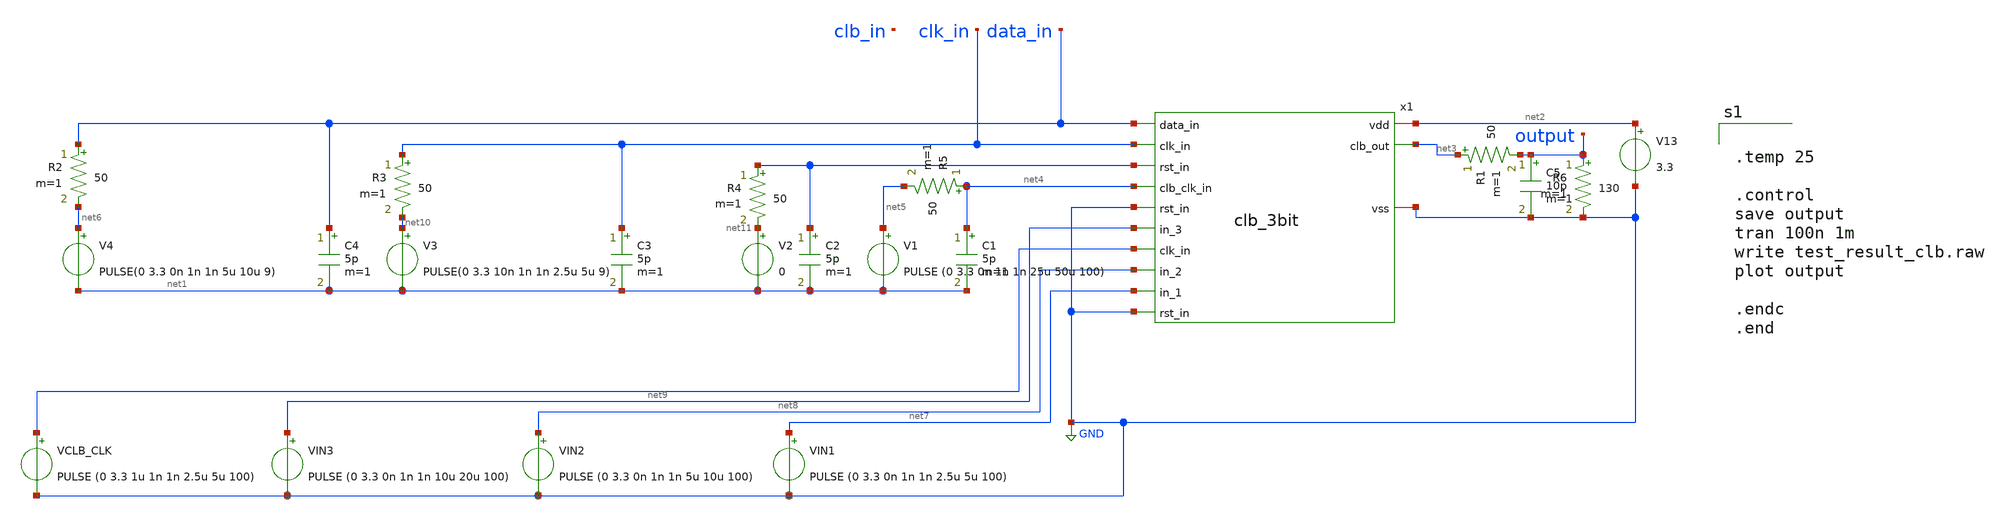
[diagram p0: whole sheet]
** sch_path: designs/digital/clb_mosbius/clb_3bit_tb.sch
**.subckt clb_3bit_tb
C1 net4 net1 5p m=1
C2 GND net1 5p m=1
C3 clk_in net1 5p m=1
C4 data_in net1 5p m=1
V1 net5 net1 PULSE (0 3.3 0n 1n 1n 25u 50u 100)
V2 net11 net1 0
V3 net10 net1 PULSE(0 3.3 10n 1n 1n 2.5u 5u 9)
V4 net6 net1 PULSE(0 3.3 0n 1n 1n 5u 10u 9)
V13 net2 GND 3.3
C5 output GND 10p m=1
R1 net3 output 50 m=1
R2 data_in net6 50 m=1
R3 clk_in net10 50 m=1
R4 GND net11 50 m=1
R5 net4 net5 50 m=1
x1 data_in clk_in net2 GND net3 net4 net9 net8 net7 GND clb_3bit
R6 output GND 130 m=1
VIN1 net7 GND PULSE (0 3.3 0n 1n 1n 2.5u 5u 100)
VIN2 net8 GND PULSE (0 3.3 0n 1n 1n 5u 10u 100)
VIN3 net9 GND PULSE (0 3.3 0n 1n 1n 10u 20u 100)
VCLB_CLK clk_in GND PULSE (0 3.3 1u 1n 1n 2.5u 5u 100)
**** begin user architecture code

.include /home/raditya/Silicons/pdks/gf180mcuD/libs.tech/ngspice/design.ngspice
.lib /home/raditya/Silicons/pdks/gf180mcuD/libs.tech/ngspice/sm141064.ngspice ff



.temp 25

.control
save output
tran 100n 1m
write test_result_clb.raw
plot output

.endc
.end


**** end user architecture code
**.ends
.GLOBAL GND
.end
